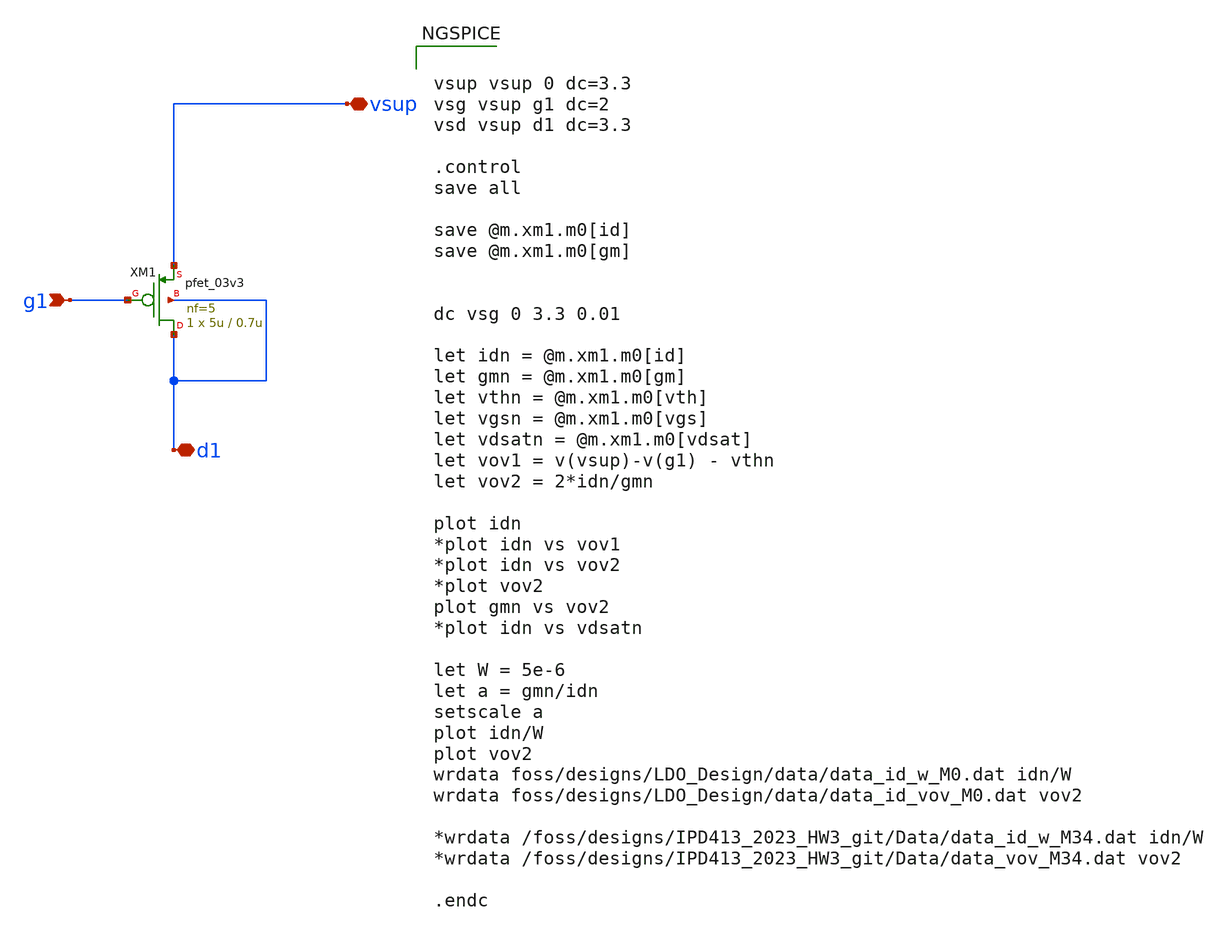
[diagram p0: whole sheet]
** sch_path: LDO/xschem/pmos-eval/pmos_charac_gf180_3p3V.sch

.include $env(PDK_ROOT)/$env(PDK)/libs.tech/ngspice/design.ngspice

.lib $env(PDK_ROOT)/$env(PDK)/libs.tech/ngspice/sm141064.ngspice typical
.lib $env(PDK_ROOT)/$env(PDK)/libs.tech/ngspice/sm141064.ngspice mimcap_statistical
.lib $env(PDK_ROOT)/$env(PDK)/libs.tech/ngspice/sm141064.ngspice cap_mim
.lib $env(PDK_ROOT)/$env(PDK)/libs.tech/ngspice/sm141064.ngspice res_typical
.lib $env(PDK_ROOT)/$env(PDK)/libs.tech/ngspice/sm141064.ngspice bjt_typical
.lib $env(PDK_ROOT)/$env(PDK)/libs.tech/ngspice/sm141064.ngspice moscap_typical


**.subckt pmos_charac_gf180_3p3V g1 d1 vsup
*.ipin g1
*.iopin d1
*.iopin vsup
XM1 d1 g1 vsup d1 pfet_03v3 L=0.7u W=5u nf=5 ad='int((nf+1)/2) * W/nf * 0.18u' as='int((nf+2)/2) * W/nf * 0.18u'
+ pd='2*int((nf+1)/2) * (W/nf + 0.18u)' ps='2*int((nf+2)/2) * (W/nf + 0.18u)' nrd='0.18u / W' nrs='0.18u / W'
+ sa=0 sb=0 sd=0 m=1
**** begin user architecture code


vsup vsup 0 dc=3.3
vsg vsup g1 dc=2
vsd vsup d1 dc=3.3

.control
save all

save @m.xm1.m0[id]
save @m.xm1.m0[gm]


dc vsg 0 3.3 0.01

let idn = @m.xm1.m0[id]
let gmn = @m.xm1.m0[gm]
let vthn = @m.xm1.m0[vth]
let vgsn = @m.xm1.m0[vgs]
let vdsatn = @m.xm1.m0[vdsat]
let vov1 = v(vsup)-v(g1) - vthn
let vov2 = 2*idn/gmn

plot idn
*plot idn vs vov1
*plot idn vs vov2
*plot vov2
plot gmn vs vov2
*plot idn vs vdsatn

let W = 5e-6
let a = gmn/idn
setscale a
plot idn/W
plot vov2
wrdata foss/designs/LDO_Design/data/data_id_w_M0.dat idn/W
wrdata foss/designs/LDO_Design/data/data_id_vov_M0.dat vov2

*wrdata /foss/designs/IPD413_2023_HW3_git/Data/data_id_w_M34.dat idn/W
*wrdata /foss/designs/IPD413_2023_HW3_git/Data/data_vov_M34.dat vov2

.endc


**** end user architecture code
**.ends
.end
